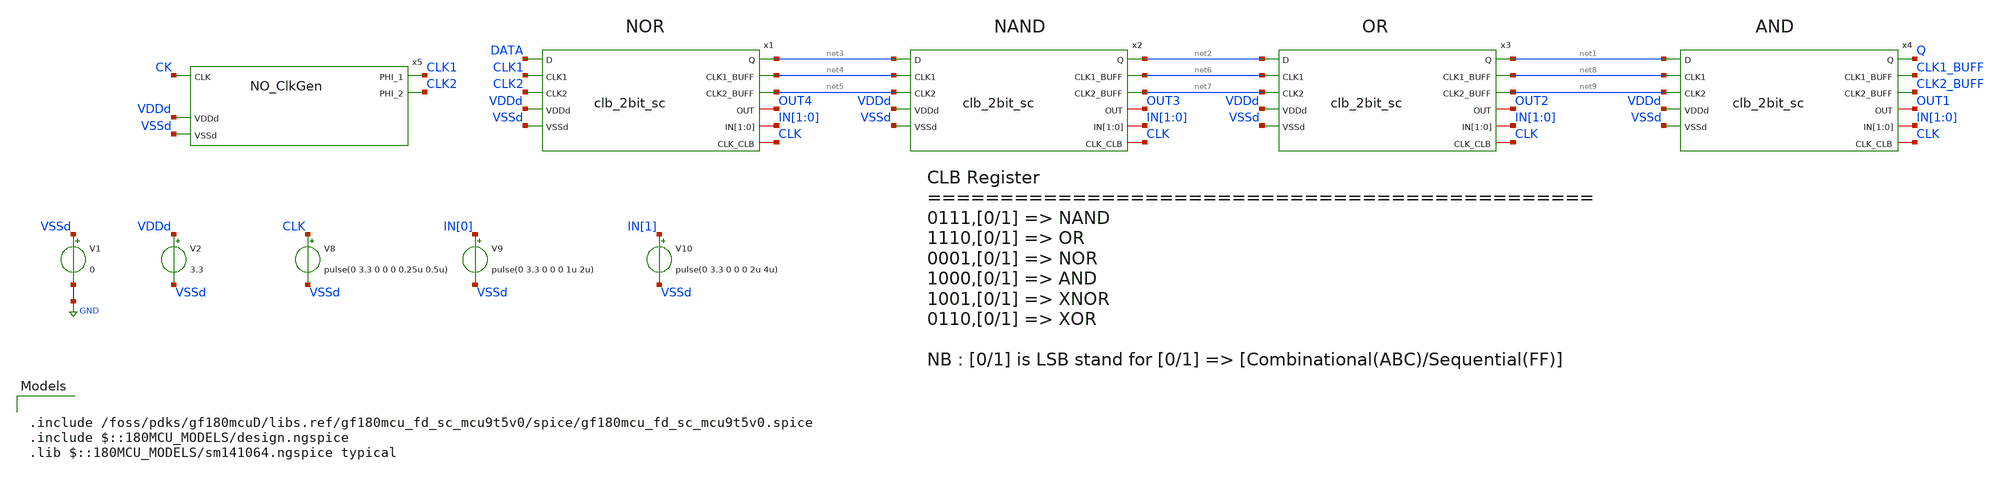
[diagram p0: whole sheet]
** sch_path: designs/libs/tb_fpga/tb_clb/tb_clb.sch
**.subckt tb_clb
V1 VSSd GND 0
V2 VDDd VSSd 3.3
V8 CLK VSSd pulse(0 3.3 0 0 0 0.25u 0.5u)
V9 IN[0] VSSd pulse(0 3.3 0 0 0 1u 2u)
V10 IN[1] VSSd pulse(0 3.3 0 0 0 2u 4u)
x5 CLK2 CK CLK1 VDDd VSSd NO_ClkGen
x1 DATA CLK1 CLK2 VDDd VSSd net3 net4 net5 OUT4 IN[1] IN[0] CLK clb_2bit_sc
x2 net3 net4 net5 VDDd VSSd net2 net6 net7 OUT3 IN[1] IN[0] CLK clb_2bit_sc
x3 net2 net6 net7 VDDd VSSd net1 net8 net9 OUT2 IN[1] IN[0] CLK clb_2bit_sc
x4 net1 net8 net9 VDDd VSSd Q CLK1_BUFF CLK2_BUFF OUT1 IN[1] IN[0] CLK clb_2bit_sc
**** begin user architecture code


* clock
abit [ bit_node ]  input_vector
.model input_vector
+ d_source(input_file="/foss/designs/sscs-chipathon2025-LNA/designs/libs/tb_fpga/tb_clb/data.txt")
* data
aclock [ clock_node ] clock_vector
.model clock_vector
+ d_source(input_file="/foss/designs/sscs-chipathon2025-LNA/designs/libs/tb_fpga/tb_clb/data_clk.txt")
* convert digital signals to analog
aconvert [ bit_node clock_node ] [ data ck ] dac_in
.model dac_in dac_bridge (out_low=0V out_high=3.3V t_rise=0.2ns t_fall=0.2ns)

.control
    save all
    TRAN 0.2n 10u
    write tb_clb.raw
    quit
.endc



.include /foss/pdks/gf180mcuD/libs.ref/gf180mcu_fd_sc_mcu9t5v0/spice/gf180mcu_fd_sc_mcu9t5v0.spice
.include $::180MCU_MODELS/design.ngspice
.lib $::180MCU_MODELS/sm141064.ngspice typical

**** end user architecture code
**.ends
.GLOBAL GND
.end
